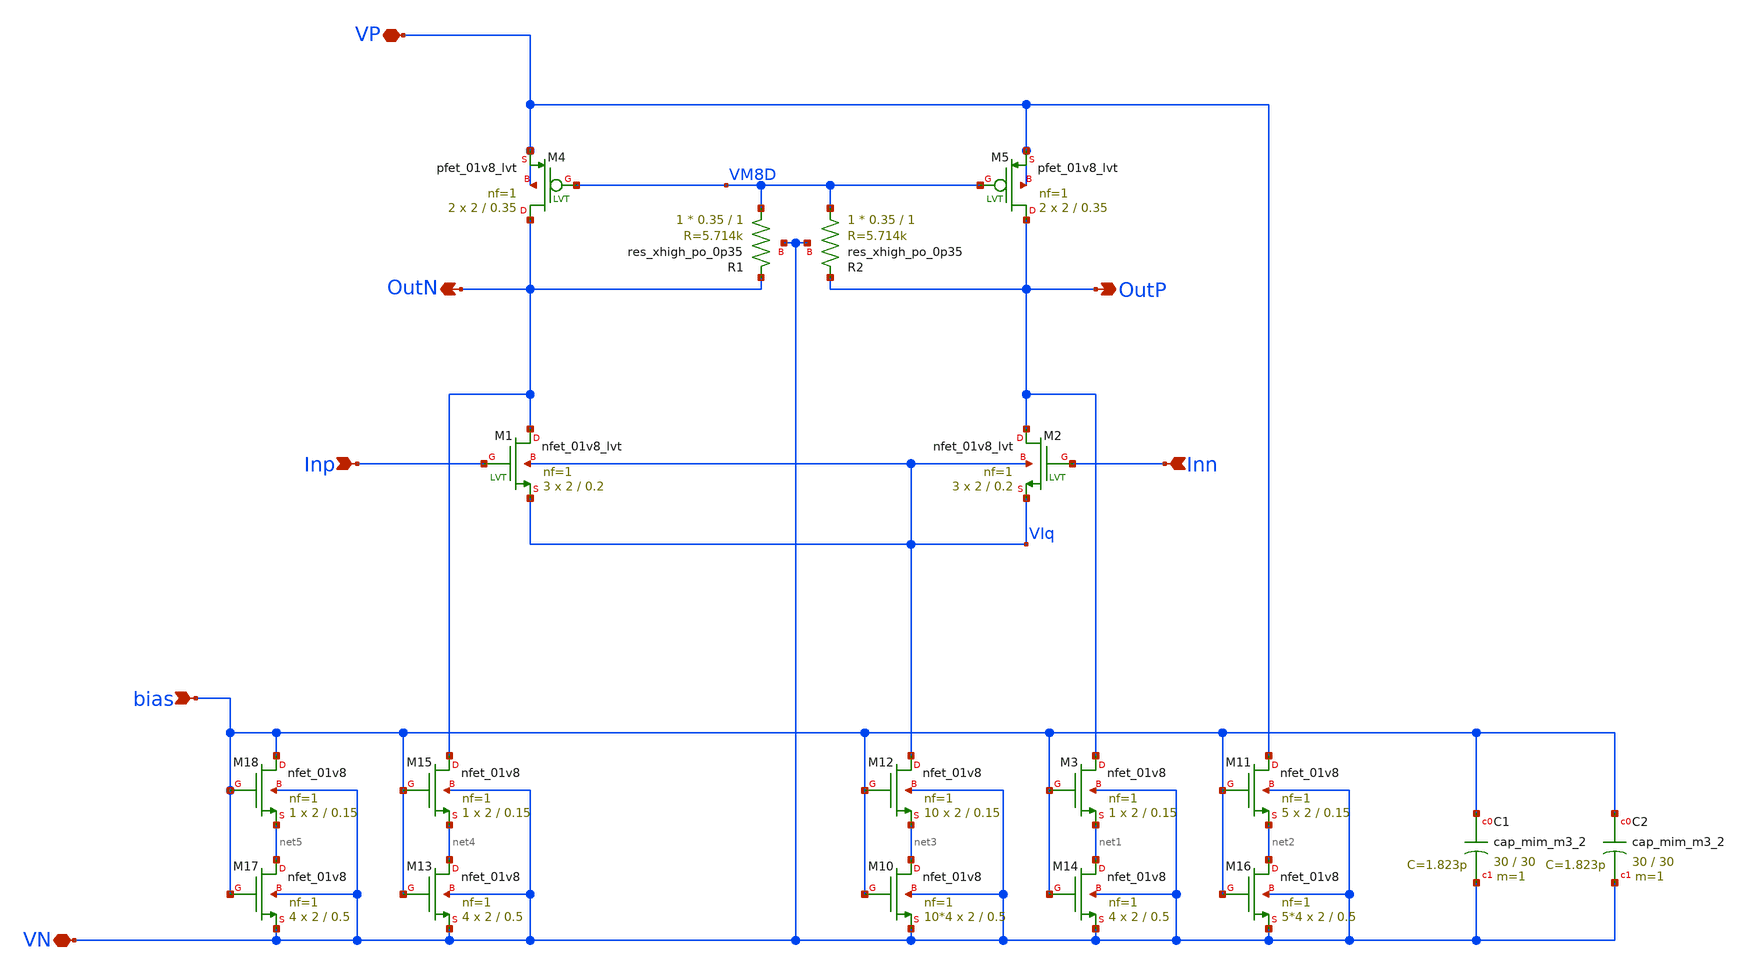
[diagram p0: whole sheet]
** sch_path: xschem/comp/compEn.sch
**.subckt compEn Inp bias Inn VP VN OutN OutP
*.ipin Inp
*.ipin bias
*.ipin Inn
*.iopin VP
*.iopin VN
*.opin OutN
*.opin OutP
XM1 OutN Inp VIq VIq sky130_fd_pr__nfet_01v8_lvt L=0.2 W=2 nf=1 ad='int((nf+1)/2) * W/nf * 0.29' as='int((nf+2)/2) * W/nf * 0.29'
+ pd='2*int((nf+1)/2) * (W/nf + 0.29)' ps='2*int((nf+2)/2) * (W/nf + 0.29)' nrd='0.29 / W' nrs='0.29 / W'
+ sa=0 sb=0 sd=0 mult=3 m=3
XM2 OutP Inn VIq VIq sky130_fd_pr__nfet_01v8_lvt L=0.2 W=2 nf=1 ad='int((nf+1)/2) * W/nf * 0.29' as='int((nf+2)/2) * W/nf * 0.29'
+ pd='2*int((nf+1)/2) * (W/nf + 0.29)' ps='2*int((nf+2)/2) * (W/nf + 0.29)' nrd='0.29 / W' nrs='0.29 / W'
+ sa=0 sb=0 sd=0 mult=3 m=3
XM14 net1 bias VN VN sky130_fd_pr__nfet_01v8 L=0.5 W=2 nf=1 ad='int((nf+1)/2) * W/nf * 0.29' as='int((nf+2)/2) * W/nf * 0.29'
+ pd='2*int((nf+1)/2) * (W/nf + 0.29)' ps='2*int((nf+2)/2) * (W/nf + 0.29)' nrd='0.29 / W' nrs='0.29 / W'
+ sa=0 sb=0 sd=0 mult=4 m=4
XM16 net2 bias VN VN sky130_fd_pr__nfet_01v8 L=0.5 W=2 nf=1 ad='int((nf+1)/2) * W/nf * 0.29' as='int((nf+2)/2) * W/nf * 0.29'
+ pd='2*int((nf+1)/2) * (W/nf + 0.29)' ps='2*int((nf+2)/2) * (W/nf + 0.29)' nrd='0.29 / W' nrs='0.29 / W'
+ sa=0 sb=0 sd=0 mult=5*4 m=5*4
XM11 VP bias net2 VN sky130_fd_pr__nfet_01v8 L=0.15 W=2 nf=1 ad='int((nf+1)/2) * W/nf * 0.29' as='int((nf+2)/2) * W/nf * 0.29'
+ pd='2*int((nf+1)/2) * (W/nf + 0.29)' ps='2*int((nf+2)/2) * (W/nf + 0.29)' nrd='0.29 / W' nrs='0.29 / W'
+ sa=0 sb=0 sd=0 mult=5 m=5
XM3 OutP bias net1 VN sky130_fd_pr__nfet_01v8 L=0.15 W=2 nf=1 ad='int((nf+1)/2) * W/nf * 0.29' as='int((nf+2)/2) * W/nf * 0.29'
+ pd='2*int((nf+1)/2) * (W/nf + 0.29)' ps='2*int((nf+2)/2) * (W/nf + 0.29)' nrd='0.29 / W' nrs='0.29 / W'
+ sa=0 sb=0 sd=0 mult=1 m=1
XM10 net3 bias VN VN sky130_fd_pr__nfet_01v8 L=0.5 W=2 nf=1 ad='int((nf+1)/2) * W/nf * 0.29' as='int((nf+2)/2) * W/nf * 0.29'
+ pd='2*int((nf+1)/2) * (W/nf + 0.29)' ps='2*int((nf+2)/2) * (W/nf + 0.29)' nrd='0.29 / W' nrs='0.29 / W'
+ sa=0 sb=0 sd=0 mult=10*4 m=10*4
XM12 VIq bias net3 VN sky130_fd_pr__nfet_01v8 L=0.15 W=2 nf=1 ad='int((nf+1)/2) * W/nf * 0.29' as='int((nf+2)/2) * W/nf * 0.29'
+ pd='2*int((nf+1)/2) * (W/nf + 0.29)' ps='2*int((nf+2)/2) * (W/nf + 0.29)' nrd='0.29 / W' nrs='0.29 / W'
+ sa=0 sb=0 sd=0 mult=10 m=10
XM13 net4 bias VN VN sky130_fd_pr__nfet_01v8 L=0.5 W=2 nf=1 ad='int((nf+1)/2) * W/nf * 0.29' as='int((nf+2)/2) * W/nf * 0.29'
+ pd='2*int((nf+1)/2) * (W/nf + 0.29)' ps='2*int((nf+2)/2) * (W/nf + 0.29)' nrd='0.29 / W' nrs='0.29 / W'
+ sa=0 sb=0 sd=0 mult=4 m=4
XM15 OutN bias net4 VN sky130_fd_pr__nfet_01v8 L=0.15 W=2 nf=1 ad='int((nf+1)/2) * W/nf * 0.29' as='int((nf+2)/2) * W/nf * 0.29'
+ pd='2*int((nf+1)/2) * (W/nf + 0.29)' ps='2*int((nf+2)/2) * (W/nf + 0.29)' nrd='0.29 / W' nrs='0.29 / W'
+ sa=0 sb=0 sd=0 mult=1 m=1
XM17 net5 bias VN VN sky130_fd_pr__nfet_01v8 L=0.5 W=2 nf=1 ad='int((nf+1)/2) * W/nf * 0.29' as='int((nf+2)/2) * W/nf * 0.29'
+ pd='2*int((nf+1)/2) * (W/nf + 0.29)' ps='2*int((nf+2)/2) * (W/nf + 0.29)' nrd='0.29 / W' nrs='0.29 / W'
+ sa=0 sb=0 sd=0 mult=4 m=4
XM18 bias bias net5 VN sky130_fd_pr__nfet_01v8 L=0.15 W=2 nf=1 ad='int((nf+1)/2) * W/nf * 0.29' as='int((nf+2)/2) * W/nf * 0.29'
+ pd='2*int((nf+1)/2) * (W/nf + 0.29)' ps='2*int((nf+2)/2) * (W/nf + 0.29)' nrd='0.29 / W' nrs='0.29 / W'
+ sa=0 sb=0 sd=0 mult=1 m=1
XC1 bias VN sky130_fd_pr__cap_mim_m3_2 W=30 L=30 MF=1 m=1
XC2 bias VN sky130_fd_pr__cap_mim_m3_2 W=30 L=30 MF=1 m=1
XR1 VM8D OutN VN sky130_fd_pr__res_xhigh_po_0p35 L=1 mult=1 m=1
XR2 VM8D OutP VN sky130_fd_pr__res_xhigh_po_0p35 L=1 mult=1 m=1
XM5 OutP VM8D VP VP sky130_fd_pr__pfet_01v8_lvt L=0.35 W=2 nf=1 ad='int((nf+1)/2) * W/nf * 0.29' as='int((nf+2)/2) * W/nf * 0.29'
+ pd='2*int((nf+1)/2) * (W/nf + 0.29)' ps='2*int((nf+2)/2) * (W/nf + 0.29)' nrd='0.29 / W' nrs='0.29 / W'
+ sa=0 sb=0 sd=0 mult=2 m=2
XM4 OutN VM8D VP VP sky130_fd_pr__pfet_01v8_lvt L=0.35 W=2 nf=1 ad='int((nf+1)/2) * W/nf * 0.29' as='int((nf+2)/2) * W/nf * 0.29'
+ pd='2*int((nf+1)/2) * (W/nf + 0.29)' ps='2*int((nf+2)/2) * (W/nf + 0.29)' nrd='0.29 / W' nrs='0.29 / W'
+ sa=0 sb=0 sd=0 mult=2 m=2
**** begin user architecture code

*.lib $::SKYWATER_MODELS/sky130.lib.spice tt
.lib $::SKYWATER_MODELS/sky130.lib.spice.tt.red tt



*.options savecurrents
.option warn=1
.control
set wr_vecnames
set wr_singlescale
* Power consumption
op
* save all
* #OP#
print @m.xm1.msky130_fd_pr__nfet_01v8_lvt[gds]
print vdd#branch
print v(vm2d)
print v(vm3d)
print v(UD_M5)
wrdata 'result_op.csv' vdd#branch
ac dec 10 1 10G
meas ac dc_gain_vm2d FIND vdb(vm2d) AT=1
let bw_amp_vm2d=dc_gain_vm2d-3
meas ac dc_gain_vm3d FIND vdb(vm3d) AT=1
let bw_amp_vm3d=dc_gain_vm3d-3
meas ac bw_vm2d when vdb(vm2d)=bw_amp_vm2d
meas ac bw_vm3d when vdb(vm3d)=bw_amp_vm3d
*MEAS AC phasem FIND vp(vm2d) WHEN vdb(vm2d)=0
* wrdata 'result_ac.csv' dc_gain bw
* plot vdb(vm2D) log
*
*print WM3D
run
reset
save @m.xm1.msky130_fd_pr__nfet_01v8_lvt[gds]
save @m.xm1.msky130_fd_pr__nfet_01v8_lvt[gm]
save @m.xm1.msky130_fd_pr__nfet_01v8_lvt[cgs]
save @m.xm1.msky130_fd_pr__nfet_01v8_lvt[cdg]
save @m.xm2.msky130_fd_pr__nfet_01v8_lvt[gm]
save @m.xm2.msky130_fd_pr__nfet_01v8_lvt[gds]
save @m.xm2.msky130_fd_pr__nfet_01v8_lvt[cgs]
save @m.xm2.msky130_fd_pr__nfet_01v8_lvt[cdg]
save @m.xm3.msky130_fd_pr__nfet_01v8_lvt[gm]
save @m.xm3.msky130_fd_pr__nfet_01v8_lvt[gds]
save @m.xm3.msky130_fd_pr__nfet_01v8_lvt[cgs]
save @m.xm3.msky130_fd_pr__nfet_01v8_lvt[cdg]
save @m.xm4.msky130_fd_pr__nfet_01v8_lvt[gm]
save @m.xm4.msky130_fd_pr__nfet_01v8_lvt[gds]
save @m.xm4.msky130_fd_pr__nfet_01v8_lvt[cgs]
save @m.xm4.msky130_fd_pr__nfet_01v8_lvt[cdg]
save @m.xm5.msky130_fd_pr__pfet_01v8_lvt[gm]
save @m.xm5.msky130_fd_pr__pfet_01v8_lvt[gds]
save @m.xm5.msky130_fd_pr__pfet_01v8_lvt[cgs]
save @m.xm5.msky130_fd_pr__pfet_01v8_lvt[cdg]
save @m.xm6.msky130_fd_pr__pfet_01v8_lvt[gm]
save @m.xm6.msky130_fd_pr__pfet_01v8_lvt[gds]
save @m.xm6.msky130_fd_pr__pfet_01v8_lvt[cgs]
save @m.xm6.msky130_fd_pr__pfet_01v8_lvt[cdg]
save @m.xm7.msky130_fd_pr__nfet_01v8_lvt[gm]
save @m.xm7.msky130_fd_pr__nfet_01v8_lvt[gds]
save @m.xm7.msky130_fd_pr__nfet_01v8_lvt[cgs]
save @m.xm7.msky130_fd_pr__nfet_01v8_lvt[cdg]
save @m.xm8.msky130_fd_pr__nfet_01v8_lvt[gm]
save @m.xm8.msky130_fd_pr__nfet_01v8_lvt[gds]
save @m.xm8.msky130_fd_pr__nfet_01v8_lvt[cgs]
save @m.xm8.msky130_fd_pr__nfet_01v8_lvt[cdg]
save @m.xm9.msky130_fd_pr__nfet_01v8_lvt[gm]
save @m.xm9.msky130_fd_pr__nfet_01v8_lvt[gds]
save @m.xm9.msky130_fd_pr__nfet_01v8_lvt[cgs]
save @m.xm9.msky130_fd_pr__nfet_01v8_lvt[cdg]
save v(Voutp)
save v(Voutn)
save v(VIa)
save v(VIq)

save v(Vinn)
save v(Vinp)
save v(VM8G)

op
write comp.raw
run
*reset
*noise v(vm1d) I1 dec 100 1 10G
*print all
*setplot noise2
*write noise2.raw
*run
reset
ac dec 10 1 1T
plot vdb(Voutp) vdb(Voutn)
plot phase(Voutp)/pi*180 phase(Voutn)/pi*180
run
reset
tran 1ps 10ns
plot v(Vinp) v(Voutn) v(Voutp)
run
.endc


**** end user architecture code
**.ends
.end
